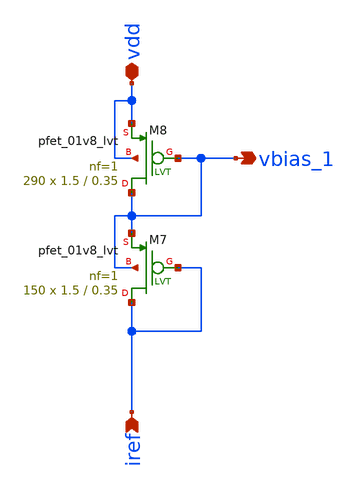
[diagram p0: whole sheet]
** sch_path: track_analogico/bias/sch/bias_reference.sch
**.subckt bias_reference iref vbias_1 vdd
*.ipin iref
*.opin vbias_1
*.iopin vdd
XM7 iref iref vbias_1 vbias_1 sky130_fd_pr__pfet_01v8_lvt L=0.35 W=1.5 nf=1 ad='int((nf+1)/2) * W/nf * 0.29'
+ as='int((nf+2)/2) * W/nf * 0.29' pd='2*int((nf+1)/2) * (W/nf + 0.29)' ps='2*int((nf+2)/2) * (W/nf + 0.29)'
+ nrd='0.29 / W' nrs='0.29 / W' sa=0 sb=0 sd=0 mult=150 m=150
XM8 vbias_1 vbias_1 vdd vdd sky130_fd_pr__pfet_01v8_lvt L=0.35 W=1.5 nf=1 ad='int((nf+1)/2) * W/nf * 0.29'
+ as='int((nf+2)/2) * W/nf * 0.29' pd='2*int((nf+1)/2) * (W/nf + 0.29)' ps='2*int((nf+2)/2) * (W/nf + 0.29)'
+ nrd='0.29 / W' nrs='0.29 / W' sa=0 sb=0 sd=0 mult=290 m=290
**.ends
.end
